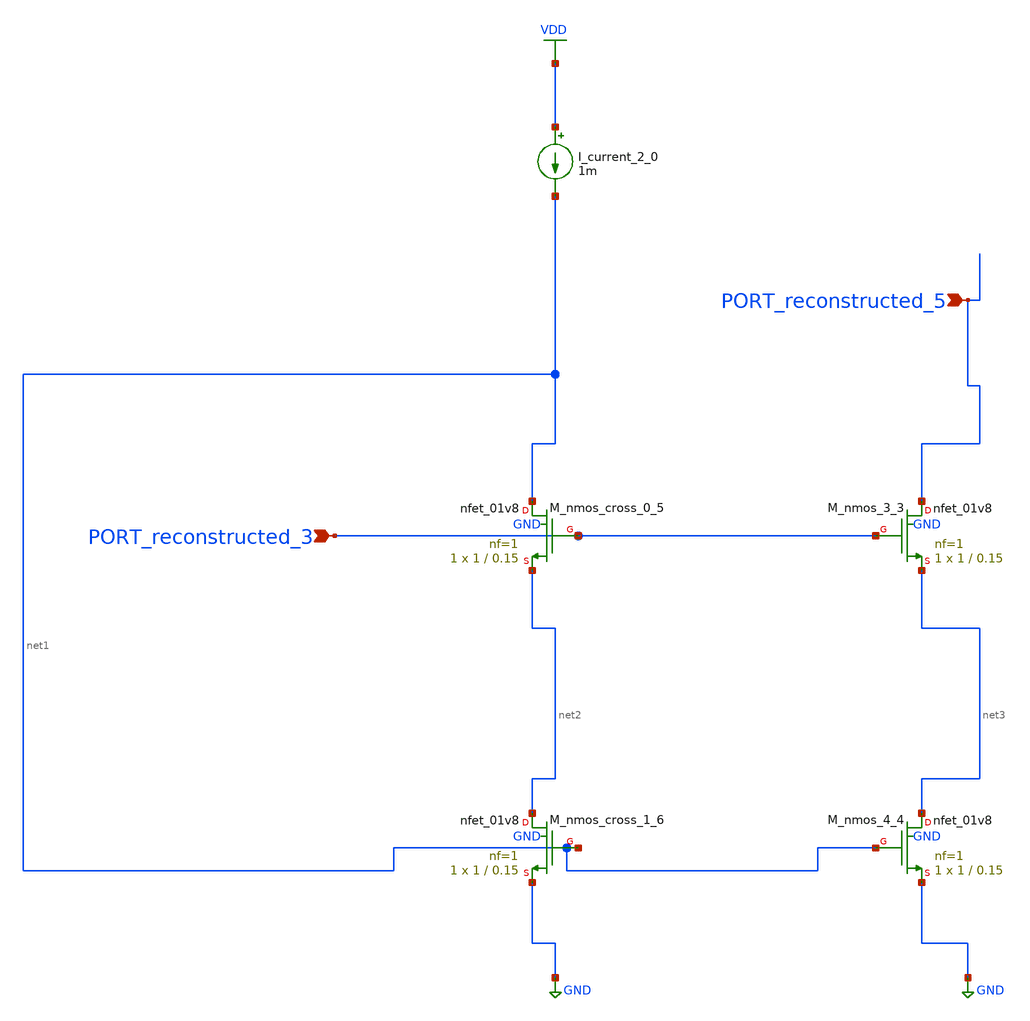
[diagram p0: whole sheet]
** sch_path: schematics/AMSNet/264.sch
**.subckt 264 PORT_reconstructed_3 PORT_reconstructed_5
*.ipin PORT_reconstructed_3
*.ipin PORT_reconstructed_5
I_current_2_0 VDD net1 1m
XM_nmos_3_3 PORT_reconstructed_5 PORT_reconstructed_3 net3 GND sky130_fd_pr__nfet_01v8 L=0.15 W=1 nf=1
+ ad='int((1 + 1)/2) * 1 / 1 * 0.29' as='int((1 + 2)/2) * 1 / 1 * 0.29' pd='2*int((1 + 1)/2) * (1 / 1 + 0.29)'
+ ps='2*int((1 + 2)/2) * (1 / 1 + 0.29)' nrd='0.29 / 1 ' nrs='0.29 / 1 ' sa=0 sb=0 sd=0 mult=1 m=1
XM_nmos_4_4 net3 net1 GND GND sky130_fd_pr__nfet_01v8 L=0.15 W=1 nf=1 ad='int((1 + 1)/2) * 1 / 1 * 0.29'
+ as='int((1 + 2)/2) * 1 / 1 * 0.29' pd='2*int((1 + 1)/2) * (1 / 1 + 0.29)' ps='2*int((1 + 2)/2) * (1 / 1 + 0.29)'
+ nrd='0.29 / 1 ' nrs='0.29 / 1 ' sa=0 sb=0 sd=0 mult=1 m=1
XM_nmos_cross_0_5 net1 PORT_reconstructed_3 net2 GND sky130_fd_pr__nfet_01v8 L=0.15 W=1 nf=1 ad='int((1 + 1)/2) * 1 / 1 * 0.29'
+ as='int((1 + 2)/2) * 1 / 1 * 0.29' pd='2*int((1 + 1)/2) * (1 / 1 + 0.29)' ps='2*int((1 + 2)/2) * (1 / 1 + 0.29)'
+ nrd='0.29 / 1 ' nrs='0.29 / 1 ' sa=0 sb=0 sd=0 mult=1 m=1
XM_nmos_cross_1_6 net2 net1 GND GND sky130_fd_pr__nfet_01v8 L=0.15 W=1 nf=1 ad='int((1 + 1)/2) * 1 / 1 * 0.29'
+ as='int((1 + 2)/2) * 1 / 1 * 0.29' pd='2*int((1 + 1)/2) * (1 / 1 + 0.29)' ps='2*int((1 + 2)/2) * (1 / 1 + 0.29)'
+ nrd='0.29 / 1 ' nrs='0.29 / 1 ' sa=0 sb=0 sd=0 mult=1 m=1
**.ends
.GLOBAL GND
.GLOBAL VDD
.end
